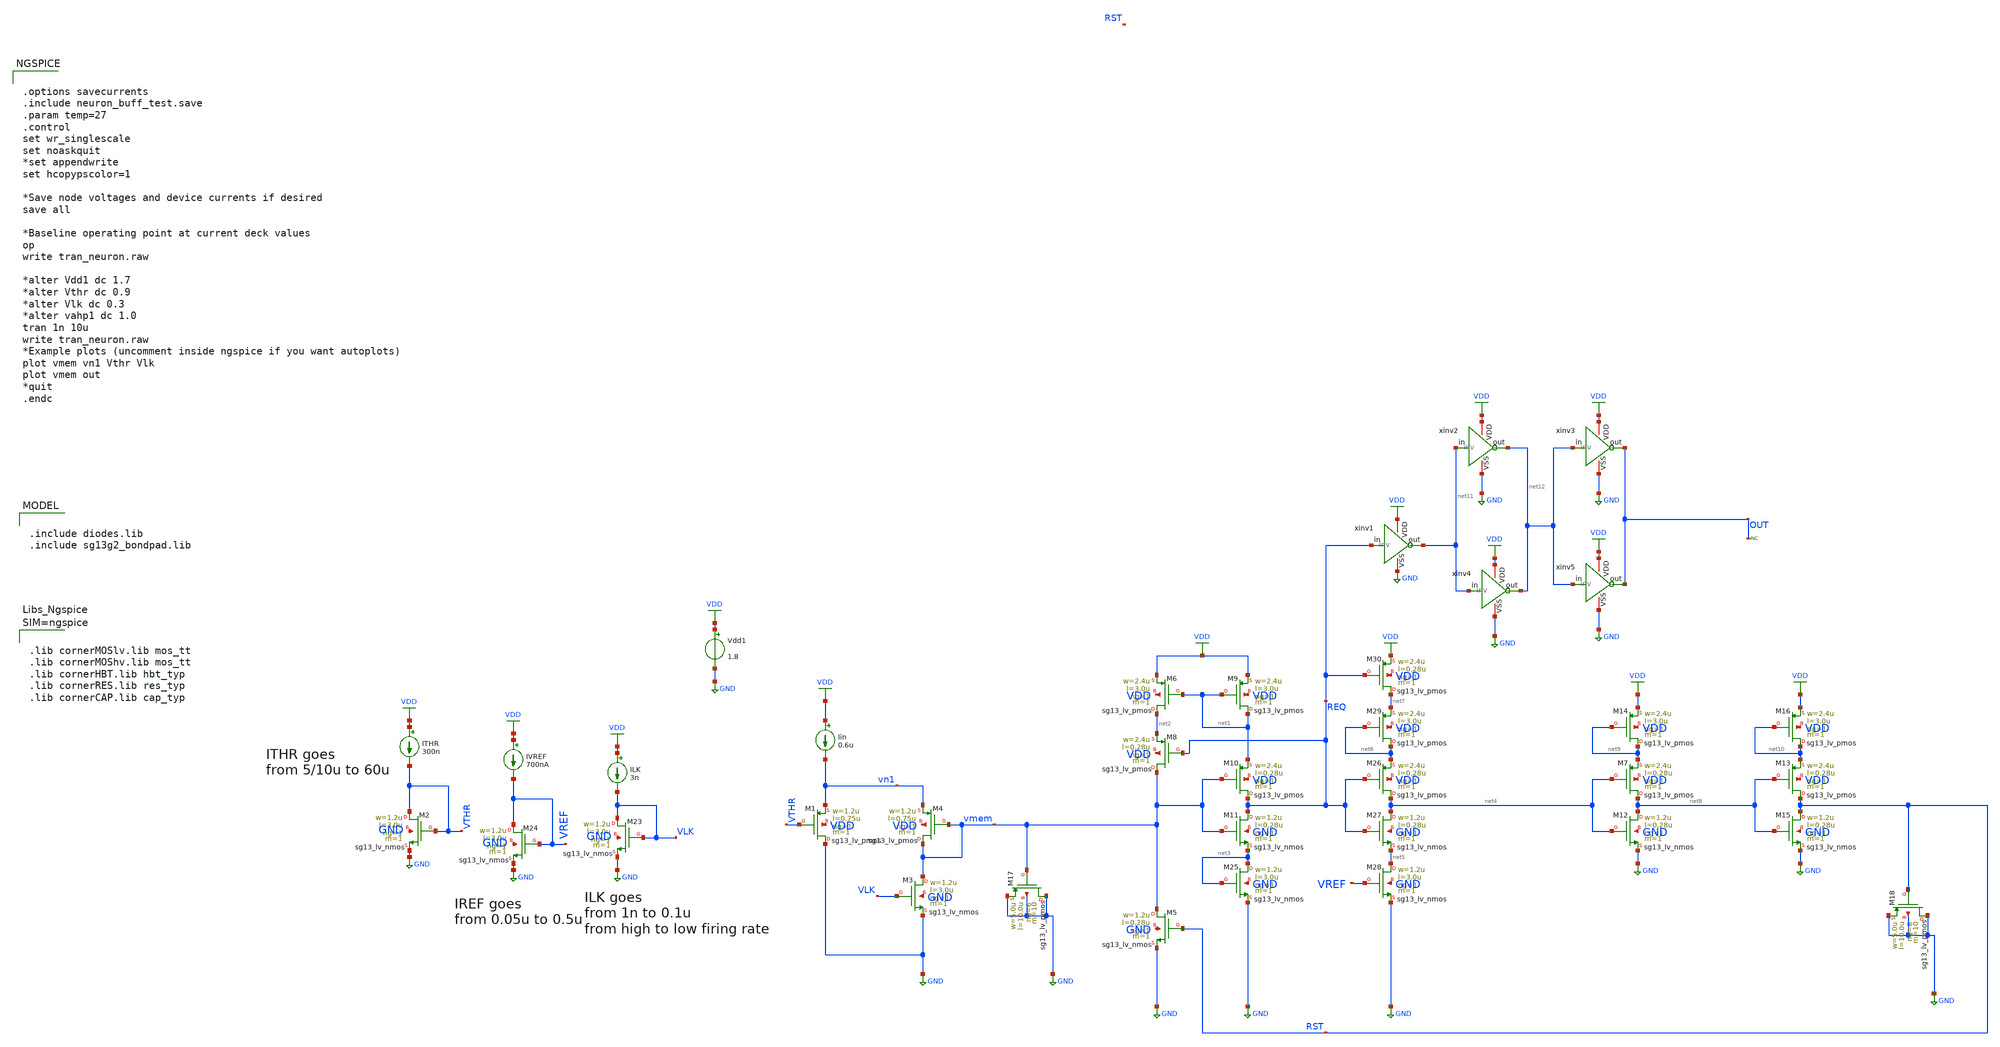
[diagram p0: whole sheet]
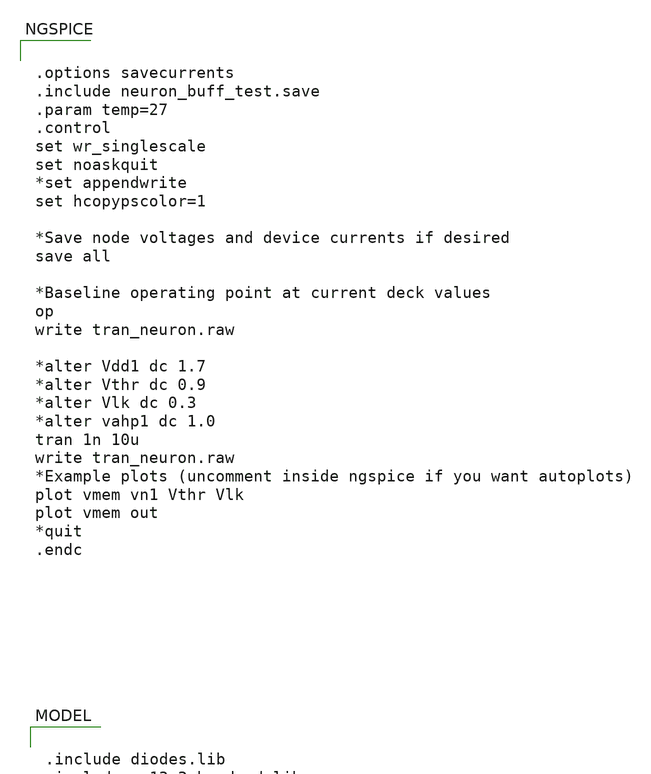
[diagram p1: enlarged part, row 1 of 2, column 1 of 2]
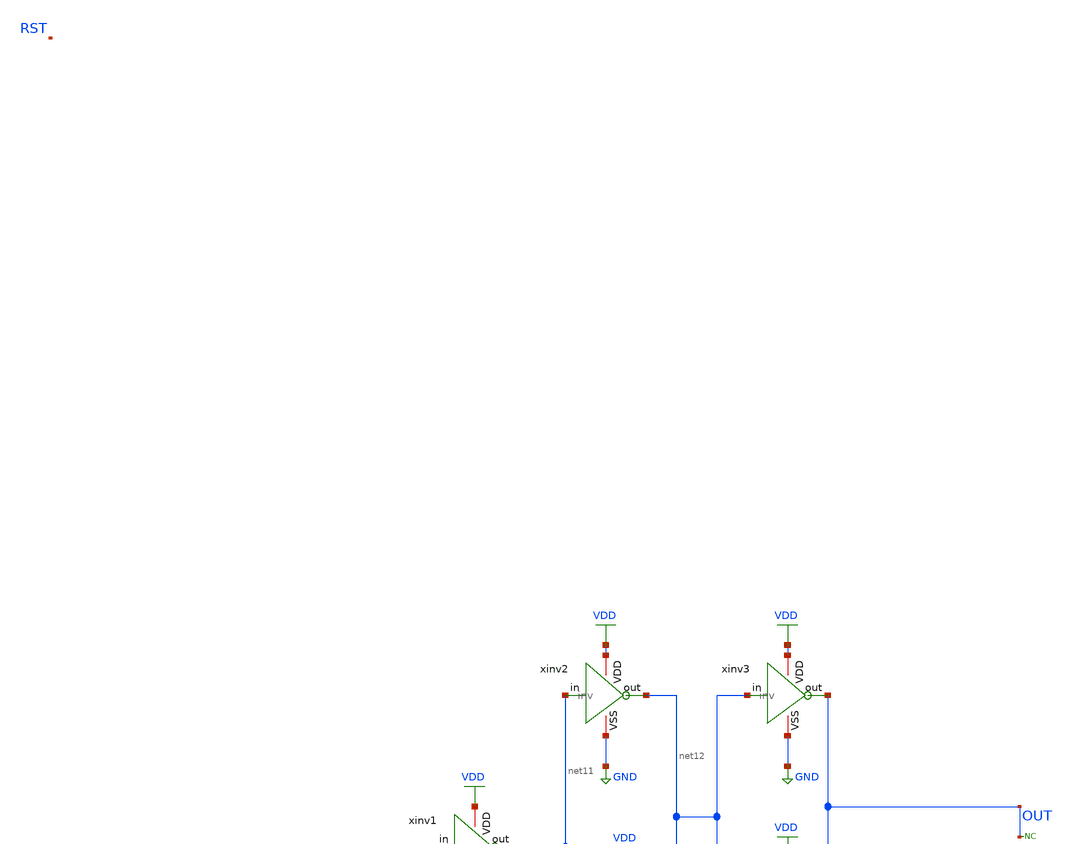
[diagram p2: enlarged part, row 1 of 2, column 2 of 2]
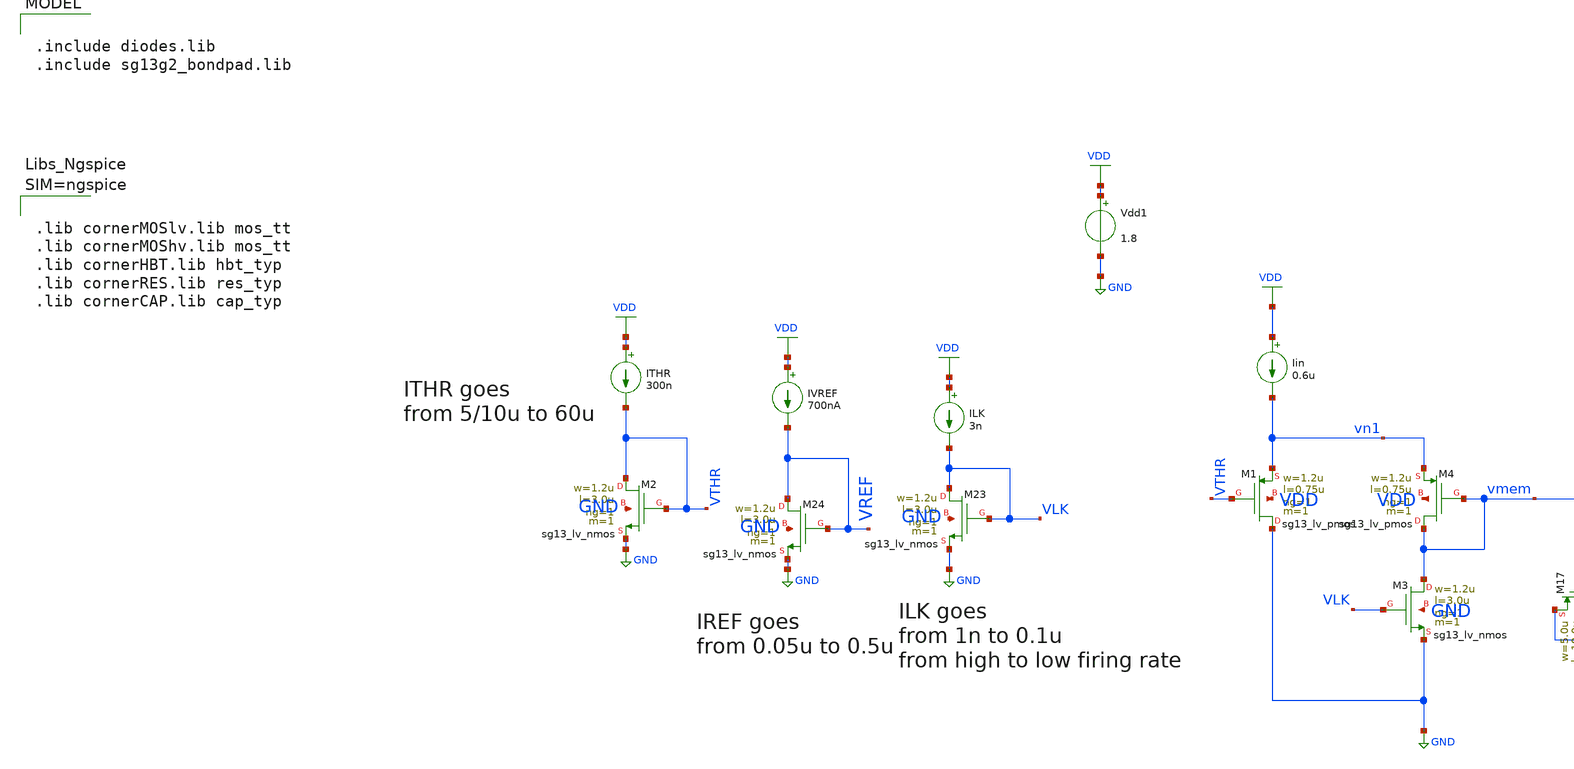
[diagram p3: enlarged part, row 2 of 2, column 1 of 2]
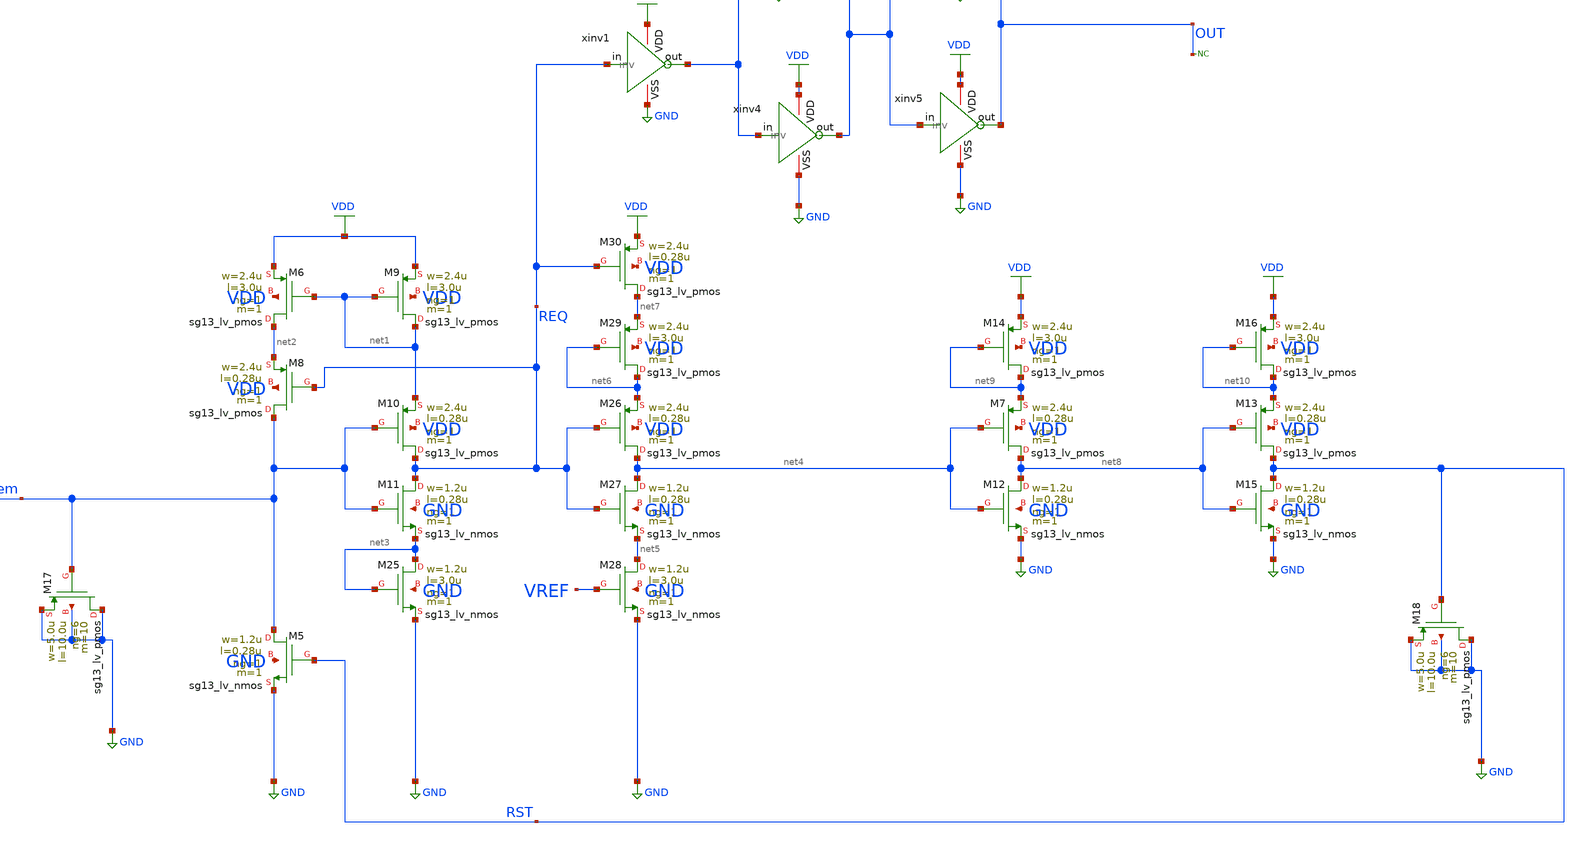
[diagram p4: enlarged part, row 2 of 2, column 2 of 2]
** sch_path: blocks/composite/dpi_adexp_neuron/design_data/xschem/dev/neuron_buff_test.sch
**.subckt neuron_buff_test
Iin VDD vn1 0.6u
XM3 vmem VLK GND GND sg13_lv_nmos w=1.2u l=3.0u ng=1 m=1 mm_ok=1
XM1 GND VTHR vn1 VDD sg13_lv_pmos w=1.2u l=0.75u ng=1 m=1 mm_ok=1
XM4 vmem vmem vn1 VDD sg13_lv_pmos w=1.2u l=0.75u ng=1 m=1 mm_ok=1
Vdd1 VDD GND 1.8
XM23 VLK VLK GND GND sg13_lv_nmos w=1.2u l=3.0u ng=1 m=1 mm_ok=1
ILK VDD VLK 3n
XM24 VREF VREF GND GND sg13_lv_nmos w=1.2u l=3.0u ng=1 m=1 mm_ok=1
IVREF VDD VREF 700nA
XM5 vmem RST GND GND sg13_lv_nmos w=1.2u l=0.28u ng=1 m=1 mm_ok=1
XM6 net2 net1 VDD VDD sg13_lv_pmos w=2.4u l=3.0u ng=1 m=1 mm_ok=1
XM8 vmem REQ net2 VDD sg13_lv_pmos w=2.4u l=0.28u ng=1 m=1 mm_ok=1
XM9 net1 net1 VDD VDD sg13_lv_pmos w=2.4u l=3.0u ng=1 m=1 mm_ok=1
XM10 REQ vmem net1 VDD sg13_lv_pmos w=2.4u l=0.28u ng=1 m=1 mm_ok=1
XM11 REQ vmem net3 GND sg13_lv_nmos w=1.2u l=0.28u ng=1 m=1 mm_ok=1
XM25 net3 net3 GND GND sg13_lv_nmos w=1.2u l=3.0u ng=1 m=1 mm_ok=1
XM26 net4 REQ net6 VDD sg13_lv_pmos w=2.4u l=0.28u ng=1 m=1 mm_ok=1
XM27 net4 REQ net5 GND sg13_lv_nmos w=1.2u l=0.28u ng=1 m=1 mm_ok=1
XM28 net5 VREF GND GND sg13_lv_nmos w=1.2u l=3.0u ng=1 m=1 mm_ok=1
XM29 net6 net6 net7 VDD sg13_lv_pmos w=2.4u l=3.0u ng=1 m=1 mm_ok=1
XM30 net7 REQ VDD VDD sg13_lv_pmos w=2.4u l=0.28u ng=1 m=1 mm_ok=1
xinv2 VDD net11 net12 GND inv
* noconn OUT
XM2 VTHR VTHR GND GND sg13_lv_nmos w=1.2u l=3.0u ng=1 m=1 mm_ok=1
ITHR VDD VTHR 300n
XM7 net8 net4 net9 VDD sg13_lv_pmos w=2.4u l=0.28u ng=1 m=1 mm_ok=1
XM12 net8 net4 GND GND sg13_lv_nmos w=1.2u l=0.28u ng=1 m=1 mm_ok=1
XM14 net9 net9 VDD VDD sg13_lv_pmos w=2.4u l=3.0u ng=1 m=1 mm_ok=1
XM13 RST net8 net10 VDD sg13_lv_pmos w=2.4u l=0.28u ng=1 m=1 mm_ok=1
XM15 RST net8 GND GND sg13_lv_nmos w=1.2u l=0.28u ng=1 m=1 mm_ok=1
XM16 net10 net10 VDD VDD sg13_lv_pmos w=2.4u l=3.0u ng=1 m=1 mm_ok=1
XM17 GND vmem GND GND sg13_lv_pmos w=5.0u l=10.0u ng=6 m=10 mm_ok=1
XM18 GND RST GND GND sg13_lv_pmos w=5.0u l=10.0u ng=6 m=10 mm_ok=1
xinv1 VDD REQ net11 GND inv
xinv3 VDD net12 OUT GND inv
xinv4 VDD net11 net12 GND inv
xinv5 VDD net12 OUT GND inv
**** begin user architecture code

.include diodes.lib
.include sg13g2_bondpad.lib



.options savecurrents
.include neuron_buff_test.save
.param temp=27
.control
set wr_singlescale
set noaskquit
*set appendwrite
set hcopypscolor=1

*Save node voltages and device currents if desired
save all

*Baseline operating point at current deck values
op
write tran_neuron.raw

*alter Vdd1 dc 1.7
*alter Vthr dc 0.9
*alter Vlk dc 0.3
*alter vahp1 dc 1.0
tran 1n 10u
write tran_neuron.raw
*Example plots (uncomment inside ngspice if you want autoplots)
plot vmem vn1 Vthr Vlk
plot vmem out
*quit
.endc





.lib cornerMOSlv.lib mos_tt
.lib cornerMOShv.lib mos_tt
.lib cornerHBT.lib hbt_typ
.lib cornerRES.lib res_typ
.lib cornerCAP.lib cap_typ



**** end user architecture code
**.ends

* expanding   symbol:  inv.sym # of pins=4
** sym_path: blocks/composite/dpi_adexp_neuron/design_data/xschem/dev/inv.sym
** sch_path: blocks/composite/dpi_adexp_neuron/design_data/xschem/dev/inv.sch
.subckt inv VDD in out VSS
*.iopin VDD
*.ipin in
*.iopin VSS
*.opin out
XM1 out in VSS VSS sg13_lv_nmos w=2.0u l=0.28u ng=1 m=1 mm_ok=1
XM2 out in VDD VDD sg13_lv_pmos w=2.0u l=0.28u ng=1 m=1 mm_ok=1
.ends

.GLOBAL GND
.GLOBAL VDD
.end
